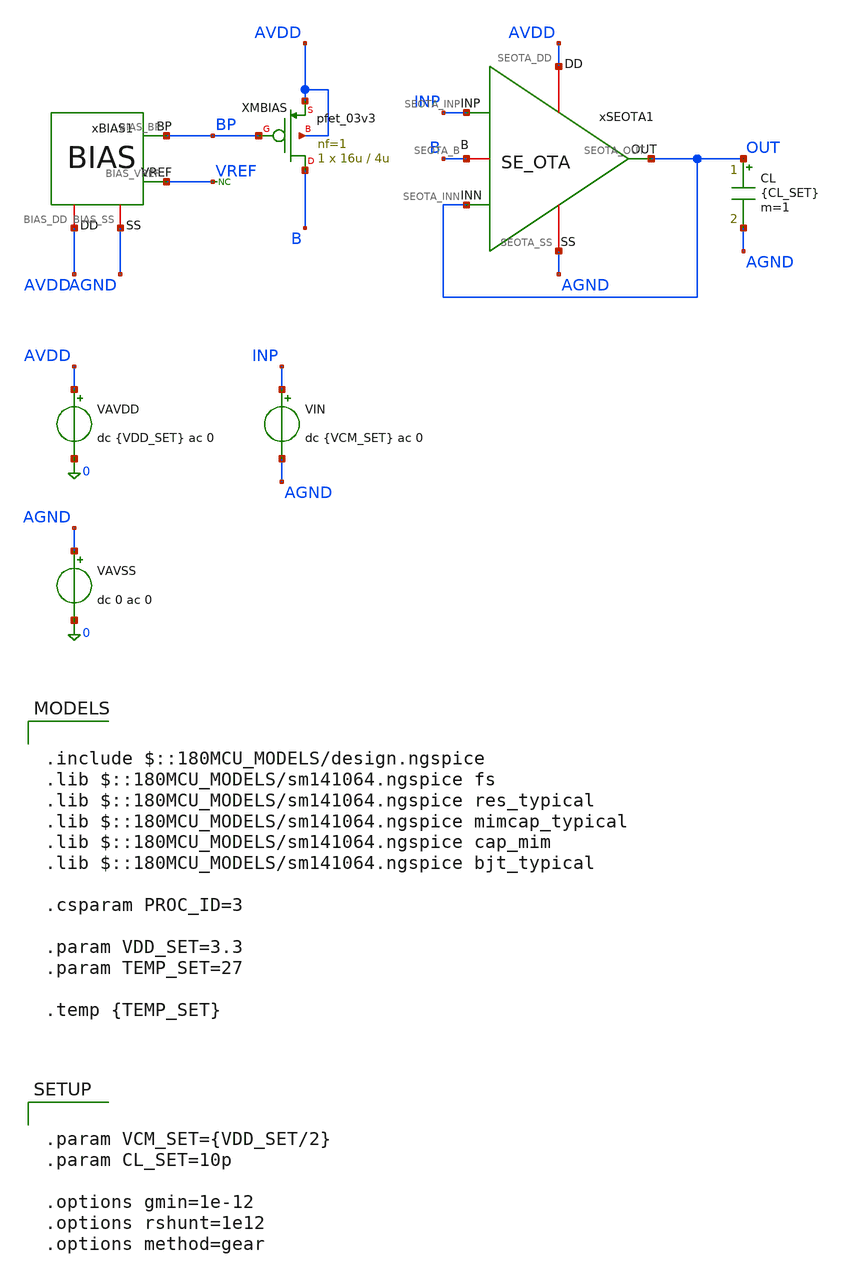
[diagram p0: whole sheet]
** sch_path: Design_Files/IC Design/Testbench/SE_OTA/Close_Loop/SE_OTA_TB_CL_FS.sch
**.subckt SE_OTA_TB_CL_FS
CL OUT AGND {CL_SET} m=1
xSEOTA1 AVDD AGND INP OUT OUT B SE_OTA
VAVDD AVDD 0 dc {VDD_SET} ac 0
.save i(vavdd)
VIN INP AGND dc {VCM_SET} ac 0
VAVSS AGND 0 dc 0 ac 0
xBIAS1 AVDD AGND BP VREF BIAS
XMBIAS B BP AVDD AVDD pfet_03v3 L=4u W=16u nf=1 ad='int((nf+1)/2) * W/nf * 0.18u' as='int((nf+2)/2) * W/nf * 0.18u'
+ pd='2*int((nf+1)/2) * (W/nf + 0.18u)' ps='2*int((nf+2)/2) * (W/nf + 0.18u)' nrd='0.18u / W' nrs='0.18u / W'
+ sa=0 sb=0 sd=0 m=1
* noconn VREF
**** begin user architecture code

.include $::180MCU_MODELS/design.ngspice
.lib $::180MCU_MODELS/sm141064.ngspice fs
.lib $::180MCU_MODELS/sm141064.ngspice res_typical
.lib $::180MCU_MODELS/sm141064.ngspice mimcap_typical
.lib $::180MCU_MODELS/sm141064.ngspice cap_mim
.lib $::180MCU_MODELS/sm141064.ngspice bjt_typical

.csparam PROC_ID=3

.param VDD_SET=3.3
.param TEMP_SET=27

.temp {TEMP_SET}




.control

destroy all

set noaskquit
set wr_singlescale
unset wr_vecnames

option klu
option numdgt=15
option method=gear
option maxord=2
option plotwinsize=0

if $&PROC_ID = 0
set proc=NOM
else
if $&PROC_ID = 1
set proc=FF
else
if $&PROC_ID = 2
set proc=SS
else
if $&PROC_ID = 3
set proc=FS
else
set proc=SF
end
end
end
end

shell mkdir -p /foss/designs/ECG_Acquisition_IC/Measurement_Results/IC_Simulation/SE_OTA/{$proc}.Result_txt
shell rm -f /foss/designs/ECG_Acquisition_IC/Measurement_Results/IC_Simulation/SE_OTA/{$proc}.Result_txt/{$proc}.cl_*.txt

foreach vddval 3.3 3.0 3.6
foreach tval 27 -40 125

if $vddval = 3.3
if $tval = 27
set case=nom
else
if $tval = -40
set case=tl
else
set case=th
end
end
else
if $vddval = 3.0
if $tval = 27
set case=vl
else
if $tval = -40
set case=vltl
else
set case=vlth
end
end
else
if $tval = 27
set case=vh
else
if $tval = -40
set case=vhtl
else
set case=vhth
end
end
end
end

alterparam VDD_SET=$vddval
alterparam TEMP_SET=$tval
reset

option klu

save all
save @m.xmbias.m0[id]

* OP

op

let vdd = v(AVDD)-v(AGND)
let vin = v(INP)-v(AGND)
let vout = v(OUT)-v(AGND)
let vin_diff = v(INP)-v(OUT)
let idd_total = abs(vavdd#branch)
let ibias = abs(@m.xmbias.m0[id])

wrdata /foss/designs/ECG_Acquisition_IC/Measurement_Results/IC_Simulation/SE_OTA/{$proc}.Result_txt/{$proc}.cl_{$case}_op.txt
+ vdd vin vout vin_diff v(B) idd_total ibias

* DC

dc VIN 0 $vddval 1m

let cl_vin = v(INP)-v(AGND)
let cl_vout = v(OUT)-v(AGND)
let cl_err = cl_vout-cl_vin
let cl_vin_diff = v(INP)-v(OUT)
let cl_idd = abs(vavdd#branch)
let cl_ibias = abs(@m.xmbias.m0[id])

setscale cl_vin

wrdata /foss/designs/ECG_Acquisition_IC/Measurement_Results/IC_Simulation/SE_OTA/{$proc}.Result_txt/{$proc}.cl_{$case}_dc.txt
+ cl_vout cl_err cl_vin_diff cl_idd cl_ibias

* TRAN

reset

option klu

save all
save @m.xmbias.m0[id]

if $vddval = 3.0
alter @VIN[PULSE]=[ 1.0 2.0 1u 10n 10n 10u 20u 0 ]
else
if $vddval = 3.3
alter @VIN[PULSE]=[ 1.15 2.15 1u 10n 10n 10u 20u 0 ]
else
alter @VIN[PULSE]=[ 1.3 2.3 1u 10n 10n 10u 20u 0 ]
end
end

tran 0.5n 30u

let tr_vin = v(INP)-v(AGND)
let tr_vout = v(OUT)-v(AGND)
let tr_err = tr_vout-tr_vin
let tr_vin_diff = v(INP)-v(OUT)
let tr_idd = abs(vavdd#branch)
let tr_ibias = abs(@m.xmbias.m0[id])

setscale time

wrdata /foss/designs/ECG_Acquisition_IC/Measurement_Results/IC_Simulation/SE_OTA/{$proc}.Result_txt/{$proc}.cl_{$case}_tran.txt
+ tr_vin tr_vout tr_err tr_vin_diff tr_idd tr_ibias

end
end

quit

.endc




.param VCM_SET={VDD_SET/2}
.param CL_SET=10p

.options gmin=1e-12
.options rshunt=1e12
.options method=gear


**** end user architecture code
**.ends

* expanding   symbol:  ECG_Acquisition_IC/Design_Files/IC Design/Schematic/SE_OTA/SE_OTA.sym # of
*+ pins=6
** sym_path: Design_Files/IC Design/Schematic/SE_OTA/SE_OTA.sym
** sch_path: Design_Files/IC Design/Schematic/SE_OTA/SE_OTA.sch
.subckt SE_OTA SEOTA_DD SEOTA_SS SEOTA_INP SEOTA_INN SEOTA_OUT SEOTA_B
*.iopin SEOTA_DD
*.iopin SEOTA_SS
*.ipin SEOTA_INP
*.ipin SEOTA_INN
*.opin SEOTA_OUT
*.iopin SEOTA_B
XM3 net4 net4 SEOTA_DD SEOTA_DD pfet_03v3 L=4u W=1u nf=1 ad='int((nf+1)/2) * W/nf * 0.18u' as='int((nf+2)/2) * W/nf * 0.18u'
+ pd='2*int((nf+1)/2) * (W/nf + 0.18u)' ps='2*int((nf+2)/2) * (W/nf + 0.18u)' nrd='0.18u / W' nrs='0.18u / W'
+ sa=0 sb=0 sd=0 m=60
XM7 SEOTA_OUT SEOTA_B SEOTA_SS SEOTA_SS nfet_03v3 L=0.5u W=1u nf=1 ad='int((nf+1)/2) * W/nf * 0.18u'
+ as='int((nf+2)/2) * W/nf * 0.18u' pd='2*int((nf+1)/2) * (W/nf + 0.18u)' ps='2*int((nf+2)/2) * (W/nf + 0.18u)'
+ nrd='0.18u / W' nrs='0.18u / W' sa=0 sb=0 sd=0 m=100
Rz net1 net2 3.8k m=1
XM5 net3 SEOTA_B SEOTA_SS SEOTA_SS nfet_03v3 L=2u W=1u nf=1 ad='int((nf+1)/2) * W/nf * 0.18u' as='int((nf+2)/2) * W/nf * 0.18u'
+ pd='2*int((nf+1)/2) * (W/nf + 0.18u)' ps='2*int((nf+2)/2) * (W/nf + 0.18u)' nrd='0.18u / W' nrs='0.18u / W'
+ sa=0 sb=0 sd=0 m=10
XM6 SEOTA_OUT net1 SEOTA_DD SEOTA_DD pfet_03v3 L=0.5u W=1u nf=1 ad='int((nf+1)/2) * W/nf * 0.18u' as='int((nf+2)/2) * W/nf * 0.18u'
+ pd='2*int((nf+1)/2) * (W/nf + 0.18u)' ps='2*int((nf+2)/2) * (W/nf + 0.18u)' nrd='0.18u / W' nrs='0.18u / W'
+ sa=0 sb=0 sd=0 m=400
XM8 SEOTA_B SEOTA_B SEOTA_SS SEOTA_SS nfet_03v3 L=2u W=1u nf=1 ad='int((nf+1)/2) * W/nf * 0.18u' as='int((nf+2)/2) * W/nf * 0.18u'
+ pd='2*int((nf+1)/2) * (W/nf + 0.18u)' ps='2*int((nf+2)/2) * (W/nf + 0.18u)' nrd='0.18u / W' nrs='0.18u / W'
+ sa=0 sb=0 sd=0 m=20
Cc net2 SEOTA_OUT 2p m=1
XM4 net1 net4 SEOTA_DD SEOTA_DD pfet_03v3 L=4u W=1u nf=1 ad='int((nf+1)/2) * W/nf * 0.18u' as='int((nf+2)/2) * W/nf * 0.18u'
+ pd='2*int((nf+1)/2) * (W/nf + 0.18u)' ps='2*int((nf+2)/2) * (W/nf + 0.18u)' nrd='0.18u / W' nrs='0.18u / W'
+ sa=0 sb=0 sd=0 m=60
XM1 net4 SEOTA_INN net3 SEOTA_SS nfet_03v3 L=4u W=1u nf=1 ad='int((nf+1)/2) * W/nf * 0.18u' as='int((nf+2)/2) * W/nf * 0.18u'
+ pd='2*int((nf+1)/2) * (W/nf + 0.18u)' ps='2*int((nf+2)/2) * (W/nf + 0.18u)' nrd='0.18u / W' nrs='0.18u / W'
+ sa=0 sb=0 sd=0 m=400
XM2 net1 SEOTA_INP net3 SEOTA_SS nfet_03v3 L=4u W=1u nf=1 ad='int((nf+1)/2) * W/nf * 0.18u' as='int((nf+2)/2) * W/nf * 0.18u'
+ pd='2*int((nf+1)/2) * (W/nf + 0.18u)' ps='2*int((nf+2)/2) * (W/nf + 0.18u)' nrd='0.18u / W' nrs='0.18u / W'
+ sa=0 sb=0 sd=0 m=400
.ends


* expanding   symbol:  ECG_Acquisition_IC/Design_Files/IC Design/Schematic/BIAS/BIAS.sym # of pins=4
** sym_path: Design_Files/IC Design/Schematic/BIAS/BIAS.sym
** sch_path: Design_Files/IC Design/Schematic/BIAS/BIAS.sch
.subckt BIAS BIAS_DD BIAS_SS BIAS_BP BIAS_VREF
*.iopin BIAS_DD
*.iopin BIAS_SS
*.opin BIAS_BP
*.opin BIAS_VREF
XMN2 BIAS_BP net2 net1 BIAS_SS nfet_03v3 L=4u W=16u nf=1 ad='int((nf+1)/2) * W/nf * 0.18u' as='int((nf+2)/2) * W/nf * 0.18u'
+ pd='2*int((nf+1)/2) * (W/nf + 0.18u)' ps='2*int((nf+2)/2) * (W/nf + 0.18u)' nrd='0.18u / W' nrs='0.18u / W'
+ sa=0 sb=0 sd=0 m=1
XMP2 BIAS_BP BIAS_BP BIAS_DD BIAS_DD pfet_03v3 L=4u W=16u nf=1 ad='int((nf+1)/2) * W/nf * 0.18u' as='int((nf+2)/2) * W/nf * 0.18u'
+ pd='2*int((nf+1)/2) * (W/nf + 0.18u)' ps='2*int((nf+2)/2) * (W/nf + 0.18u)' nrd='0.18u / W' nrs='0.18u / W'
+ sa=0 sb=0 sd=0 m=1
XMN1 net2 net2 net3 BIAS_SS nfet_03v3 L=4u W=24u nf=1 ad='int((nf+1)/2) * W/nf * 0.18u' as='int((nf+2)/2) * W/nf * 0.18u'
+ pd='2*int((nf+1)/2) * (W/nf + 0.18u)' ps='2*int((nf+2)/2) * (W/nf + 0.18u)' nrd='0.18u / W' nrs='0.18u / W'
+ sa=0 sb=0 sd=0 m=1
XMP1 net2 BIAS_BP BIAS_DD BIAS_DD pfet_03v3 L=4u W=16u nf=1 ad='int((nf+1)/2) * W/nf * 0.18u' as='int((nf+2)/2) * W/nf * 0.18u'
+ pd='2*int((nf+1)/2) * (W/nf + 0.18u)' ps='2*int((nf+2)/2) * (W/nf + 0.18u)' nrd='0.18u / W' nrs='0.18u / W'
+ sa=0 sb=0 sd=0 m=1
XMST BIAS_BP BIAS_BP net2 BIAS_SS nfet_03v3 L=10u W=0.5u nf=1 ad='int((nf+1)/2) * W/nf * 0.18u' as='int((nf+2)/2) * W/nf * 0.18u'
+ pd='2*int((nf+1)/2) * (W/nf + 0.18u)' ps='2*int((nf+2)/2) * (W/nf + 0.18u)' nrd='0.18u / W' nrs='0.18u / W'
+ sa=0 sb=0 sd=0 m=1
XRP BIAS_VREF BIAS_DD BIAS_SS ppolyf_u_2k r_width=4e-6 r_length=1000e-6 m=1
XRN BIAS_SS BIAS_VREF BIAS_SS ppolyf_u_2k r_width=4e-6 r_length=1000e-6 m=1
XCN BIAS_VREF BIAS_SS cap_mim_2f0fF c_width=70.7e-6 c_length=70.7e-6 m=1
XQ1 BIAS_SS BIAS_SS net3 pnp_05p00x00p42 m=1 par=1
XQ2 BIAS_SS BIAS_SS net4 pnp_05p00x00p42 m=30 par=30
XRS net4 net1 BIAS_SS nwell r_width=3e-6 r_length=1.522e-6 m=1
.ends

.end
